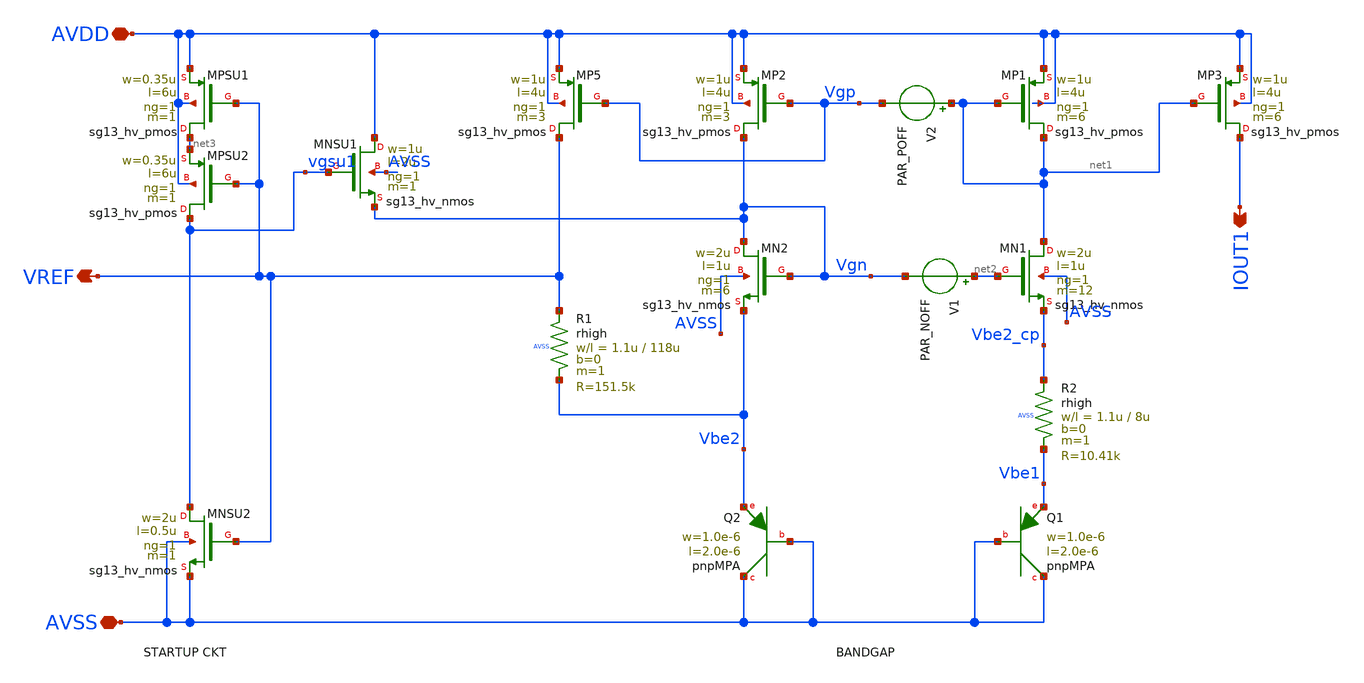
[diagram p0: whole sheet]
** sch_path: xschem/pmbgr1.sch
**.subckt pmbgr1 AVDD AVSS VREF IOUT1
*.iopin AVDD
*.iopin AVSS
*.opin VREF
*.opin IOUT1
XQ1 AVSS AVSS Vbe1 pnpMPA a=2p p=6u m=7
XQ2 AVSS AVSS Vbe2 pnpMPA a=2p p=6u m=1
XMN2 Vgn Vgn Vbe2 AVSS sg13_hv_nmos w=2u l=1u ng=1 m=6 mm_ok=1
XMN1 net1 net2 Vbe2_cp AVSS sg13_hv_nmos w=2u l=1u ng=1 m=12 mm_ok=1
XMP2 Vgn Vgp AVDD AVDD sg13_hv_pmos w=1u l=4u ng=1 m=3 mm_ok=1
XMP1 net1 net1 AVDD AVDD sg13_hv_pmos w=1u l=4u ng=1 m=6 mm_ok=1
XR2 Vbe2_cp Vbe1 AVSS rhigh w=1.1u l=8u m=1 b=0 mm_ok=1
XMP3 IOUT1 net1 AVDD AVDD sg13_hv_pmos w=1u l=4u ng=1 m=6 mm_ok=1
XMP5 VREF Vgp AVDD AVDD sg13_hv_pmos w=1u l=4u ng=1 m=3 mm_ok=1
XR1 VREF Vbe2 AVSS rhigh w=1.1u l=118u m=1 b=0 mm_ok=1
V1 net2 Vgn PAR_NOFF
V2 net1 Vgp PAR_POFF
XMNSU1 AVDD vgsu1 Vgn AVSS sg13_hv_nmos w=1u l=2u ng=1 m=1 mm_ok=1
XMPSU1 net3 VREF AVDD AVDD sg13_hv_pmos w=0.35u l=6u ng=1 m=1 mm_ok=1
XMNSU2 vgsu1 VREF AVSS AVSS sg13_hv_nmos w=2u l=0.5u ng=1 m=1 mm_ok=1
XMPSU2 vgsu1 VREF net3 AVDD sg13_hv_pmos w=0.35u l=6u ng=1 m=1 mm_ok=1
**.ends
.end
